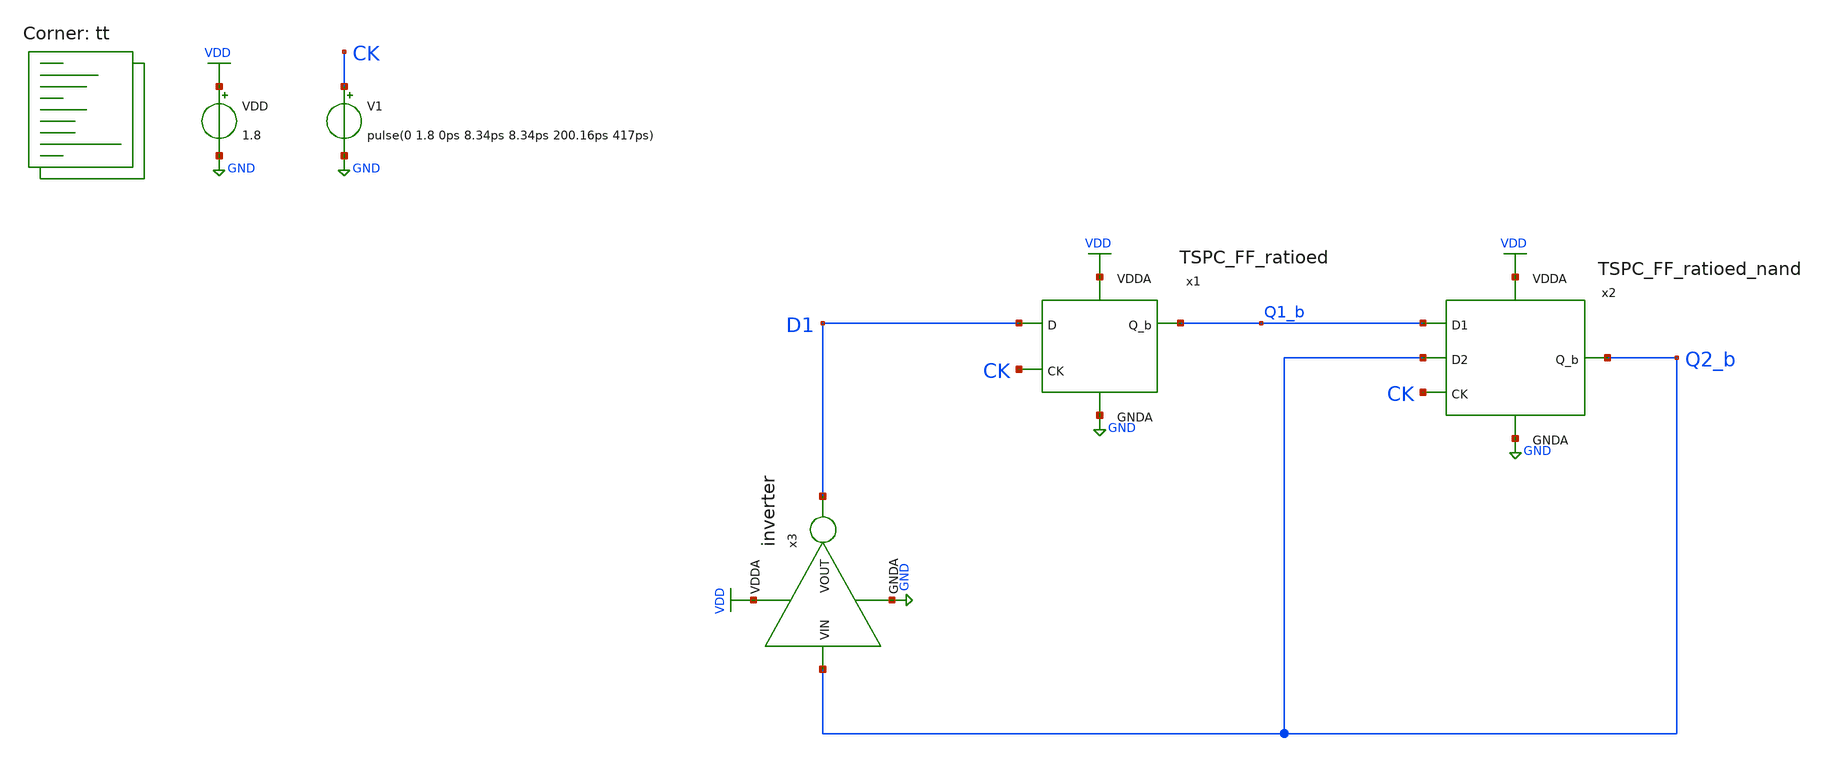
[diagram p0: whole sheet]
** sch_path: projects/pll/divider/xschem_ngspice/tb_TSPC_FF_ratioed_divide3_4.sch
**.subckt tb_TSPC_FF_ratioed_divide3_4
VDD VDD GND 1.8
V1 CK GND pulse(0 1.8 0ps 8.34ps 8.34ps 200.16ps 417ps)
x1 VDD Q1_b D1 CK GND TSPC_FF_ratioed
x2 VDD Q2_b Q2_b Q1_b CK GND TSPC_FF_ratioed_nand
x3 VDD Q2_b D1 GND inverter
**** begin user architecture code



.include /foss/pdks/sky130A/libs.ref/sky130_fd_sc_hd/spice/sky130_fd_sc_hd.spice

.option method=gear
.option wnflag=1
.option savecurrents


*.ic v(d)=0
*.ic v(q)=0
*.ic v(q1)=0

.probe p(x1) p(x2) p(x3)

.control

  * save v(d1) v(q1) v(q1_b) v(q2_b) v(a1) v(a2) v(a3) v(a4) v(b1) v(b2) v(c1) v(c2) v(c3) v(ck)
+ v(ck1) v(ck1_b)
  save all
  * tran 0.1n 1u
  tran 1p 20n

  remzerovec
  linearize v(ck) v(d1) v(q1_b) v(q2_b) p(x1:power) p(x2:power) p(x3:power)
  write tb_TSPC_FF_ratioed_divide3_4.raw
  wrdata
+ /foss/designs/my_design/projects/pll/divider/xschem_ngspice/tb_TSPC_FF_ratioed_divide3_4.txt p(x1:power) p(x2:power) p(x3:power)
  * set appendwrite

.endc



.lib $::SKYWATER_MODELS/sky130.lib.spice tt
**** end user architecture code
**.ends

* expanding   symbol:
*+  /foss/designs/my_design/projects/pll/divider/xschem_ngspice/TSPC_FF_ratioed.sym # of pins=5
** sym_path: projects/pll/divider/xschem_ngspice/TSPC_FF_ratioed.sym
** sch_path: projects/pll/divider/xschem_ngspice/TSPC_FF_ratioed.sch
.subckt TSPC_FF_ratioed VDDA Q_b D CK GNDA
*.ipin CK
*.ipin D
*.opin Q_b
*.ipin VDDA
*.ipin GNDA
XM1 Q_b CK VDDA VDDA sky130_fd_pr__pfet_01v8 L=0.15 W=1 nf=1 ad='int((nf+1)/2) * W/nf * 0.29' as='int((nf+2)/2) * W/nf * 0.29'
+ pd='2*int((nf+1)/2) * (W/nf + 0.29)' ps='2*int((nf+2)/2) * (W/nf + 0.29)' nrd='0.29 / W' nrs='0.29 / W'
+ sa=0 sb=0 sd=0 mult=1 m=1
XM2 Q_b net2 GNDA GNDA sky130_fd_pr__nfet_01v8 L=0.15 W=1 nf=1 ad='int((nf+1)/2) * W/nf * 0.29' as='int((nf+2)/2) * W/nf * 0.29'
+ pd='2*int((nf+1)/2) * (W/nf + 0.29)' ps='2*int((nf+2)/2) * (W/nf + 0.29)' nrd='0.29 / W' nrs='0.29 / W'
+ sa=0 sb=0 sd=0 mult=1 m=1
XM3 net2 net3 VDDA VDDA sky130_fd_pr__pfet_01v8 L=0.15 W=1 nf=1 ad='int((nf+1)/2) * W/nf * 0.29' as='int((nf+2)/2) * W/nf * 0.29'
+ pd='2*int((nf+1)/2) * (W/nf + 0.29)' ps='2*int((nf+2)/2) * (W/nf + 0.29)' nrd='0.29 / W' nrs='0.29 / W'
+ sa=0 sb=0 sd=0 mult=1 m=1
XM4 net2 CK GNDA GNDA sky130_fd_pr__nfet_01v8 L=0.15 W=3 nf=3 ad='int((nf+1)/2) * W/nf * 0.29' as='int((nf+2)/2) * W/nf * 0.29'
+ pd='2*int((nf+1)/2) * (W/nf + 0.29)' ps='2*int((nf+2)/2) * (W/nf + 0.29)' nrd='0.29 / W' nrs='0.29 / W'
+ sa=0 sb=0 sd=0 mult=1 m=1
XM5 net3 D VDDA VDDA sky130_fd_pr__pfet_01v8 L=0.15 W=1 nf=1 ad='int((nf+1)/2) * W/nf * 0.29' as='int((nf+2)/2) * W/nf * 0.29'
+ pd='2*int((nf+1)/2) * (W/nf + 0.29)' ps='2*int((nf+2)/2) * (W/nf + 0.29)' nrd='0.29 / W' nrs='0.29 / W'
+ sa=0 sb=0 sd=0 mult=1 m=1
XM7 net1 D GNDA GNDA sky130_fd_pr__nfet_01v8 L=0.15 W=1 nf=1 ad='int((nf+1)/2) * W/nf * 0.29' as='int((nf+2)/2) * W/nf * 0.29'
+ pd='2*int((nf+1)/2) * (W/nf + 0.29)' ps='2*int((nf+2)/2) * (W/nf + 0.29)' nrd='0.29 / W' nrs='0.29 / W'
+ sa=0 sb=0 sd=0 mult=1 m=1
XM6 net3 CK net1 GNDA sky130_fd_pr__nfet_01v8 L=0.15 W=1 nf=1 ad='int((nf+1)/2) * W/nf * 0.29' as='int((nf+2)/2) * W/nf * 0.29'
+ pd='2*int((nf+1)/2) * (W/nf + 0.29)' ps='2*int((nf+2)/2) * (W/nf + 0.29)' nrd='0.29 / W' nrs='0.29 / W'
+ sa=0 sb=0 sd=0 mult=1 m=1
.ends


* expanding   symbol:
*+  /foss/designs/my_design/projects/pll/divider/xschem_ngspice/TSPC_FF_ratioed_nand.sym # of pins=6
** sym_path: projects/pll/divider/xschem_ngspice/TSPC_FF_ratioed_nand.sym
** sch_path: projects/pll/divider/xschem_ngspice/TSPC_FF_ratioed_nand.sch
.subckt TSPC_FF_ratioed_nand VDDA Q_b D2 D1 CK GNDA
*.ipin CK
*.ipin D1
*.opin Q_b
*.ipin VDDA
*.ipin GNDA
*.ipin D2
XM1 Q_b CK VDDA VDDA sky130_fd_pr__pfet_01v8 L=0.15 W=1 nf=1 ad='int((nf+1)/2) * W/nf * 0.29' as='int((nf+2)/2) * W/nf * 0.29'
+ pd='2*int((nf+1)/2) * (W/nf + 0.29)' ps='2*int((nf+2)/2) * (W/nf + 0.29)' nrd='0.29 / W' nrs='0.29 / W'
+ sa=0 sb=0 sd=0 mult=1 m=1
XM2 Q_b B GNDA GNDA sky130_fd_pr__nfet_01v8 L=0.15 W=1 nf=1 ad='int((nf+1)/2) * W/nf * 0.29' as='int((nf+2)/2) * W/nf * 0.29'
+ pd='2*int((nf+1)/2) * (W/nf + 0.29)' ps='2*int((nf+2)/2) * (W/nf + 0.29)' nrd='0.29 / W' nrs='0.29 / W'
+ sa=0 sb=0 sd=0 mult=1 m=1
XM3 B net1 VDDA VDDA sky130_fd_pr__pfet_01v8 L=0.15 W=1 nf=1 ad='int((nf+1)/2) * W/nf * 0.29' as='int((nf+2)/2) * W/nf * 0.29'
+ pd='2*int((nf+1)/2) * (W/nf + 0.29)' ps='2*int((nf+2)/2) * (W/nf + 0.29)' nrd='0.29 / W' nrs='0.29 / W'
+ sa=0 sb=0 sd=0 mult=1 m=1
XM4 B CK GNDA GNDA sky130_fd_pr__nfet_01v8 L=0.15 W=2 nf=2 ad='int((nf+1)/2) * W/nf * 0.29' as='int((nf+2)/2) * W/nf * 0.29'
+ pd='2*int((nf+1)/2) * (W/nf + 0.29)' ps='2*int((nf+2)/2) * (W/nf + 0.29)' nrd='0.29 / W' nrs='0.29 / W'
+ sa=0 sb=0 sd=0 mult=1 m=1
XM5 net1 D2 VDDA VDDA sky130_fd_pr__pfet_01v8 L=0.15 W=2 nf=2 ad='int((nf+1)/2) * W/nf * 0.29' as='int((nf+2)/2) * W/nf * 0.29'
+ pd='2*int((nf+1)/2) * (W/nf + 0.29)' ps='2*int((nf+2)/2) * (W/nf + 0.29)' nrd='0.29 / W' nrs='0.29 / W'
+ sa=0 sb=0 sd=0 mult=1 m=1
XM9 net3 D1 GNDA GNDA sky130_fd_pr__nfet_01v8 L=0.15 W=1 nf=1 ad='int((nf+1)/2) * W/nf * 0.29' as='int((nf+2)/2) * W/nf * 0.29'
+ pd='2*int((nf+1)/2) * (W/nf + 0.29)' ps='2*int((nf+2)/2) * (W/nf + 0.29)' nrd='0.29 / W' nrs='0.29 / W'
+ sa=0 sb=0 sd=0 mult=1 m=1
XM7 net1 CK net2 GNDA sky130_fd_pr__nfet_01v8 L=0.15 W=1 nf=1 ad='int((nf+1)/2) * W/nf * 0.29' as='int((nf+2)/2) * W/nf * 0.29'
+ pd='2*int((nf+1)/2) * (W/nf + 0.29)' ps='2*int((nf+2)/2) * (W/nf + 0.29)' nrd='0.29 / W' nrs='0.29 / W'
+ sa=0 sb=0 sd=0 mult=1 m=1
XM6 net1 D1 VDDA VDDA sky130_fd_pr__pfet_01v8 L=0.15 W=2 nf=2 ad='int((nf+1)/2) * W/nf * 0.29' as='int((nf+2)/2) * W/nf * 0.29'
+ pd='2*int((nf+1)/2) * (W/nf + 0.29)' ps='2*int((nf+2)/2) * (W/nf + 0.29)' nrd='0.29 / W' nrs='0.29 / W'
+ sa=0 sb=0 sd=0 mult=1 m=1
XM8 net2 D2 net3 GNDA sky130_fd_pr__nfet_01v8 L=0.15 W=1 nf=1 ad='int((nf+1)/2) * W/nf * 0.29' as='int((nf+2)/2) * W/nf * 0.29'
+ pd='2*int((nf+1)/2) * (W/nf + 0.29)' ps='2*int((nf+2)/2) * (W/nf + 0.29)' nrd='0.29 / W' nrs='0.29 / W'
+ sa=0 sb=0 sd=0 mult=1 m=1
.ends


* expanding   symbol:  /foss/designs/my_design/projects/pll/divider/xschem_ngspice/inverter.sym # of
*+ pins=4
** sym_path: projects/pll/divider/xschem_ngspice/inverter.sym
** sch_path: projects/pll/divider/xschem_ngspice/inverter.sch
.subckt inverter VDDA VIN VOUT GNDA
*.ipin VIN
*.ipin VDDA
*.ipin GNDA
*.opin VOUT
XM31 VOUT VIN VDDA VDDA sky130_fd_pr__pfet_01v8 L=0.15 W=2 nf=2 ad='int((nf+1)/2) * W/nf * 0.29' as='int((nf+2)/2) * W/nf * 0.29'
+ pd='2*int((nf+1)/2) * (W/nf + 0.29)' ps='2*int((nf+2)/2) * (W/nf + 0.29)' nrd='0.29 / W' nrs='0.29 / W'
+ sa=0 sb=0 sd=0 mult=1 m=1
XM32 VOUT VIN GNDA GNDA sky130_fd_pr__nfet_01v8 L=0.15 W=1 nf=1 ad='int((nf+1)/2) * W/nf * 0.29' as='int((nf+2)/2) * W/nf * 0.29'
+ pd='2*int((nf+1)/2) * (W/nf + 0.29)' ps='2*int((nf+2)/2) * (W/nf + 0.29)' nrd='0.29 / W' nrs='0.29 / W'
+ sa=0 sb=0 sd=0 mult=1 m=1
.ends

.GLOBAL GND
.GLOBAL VDD
.end
